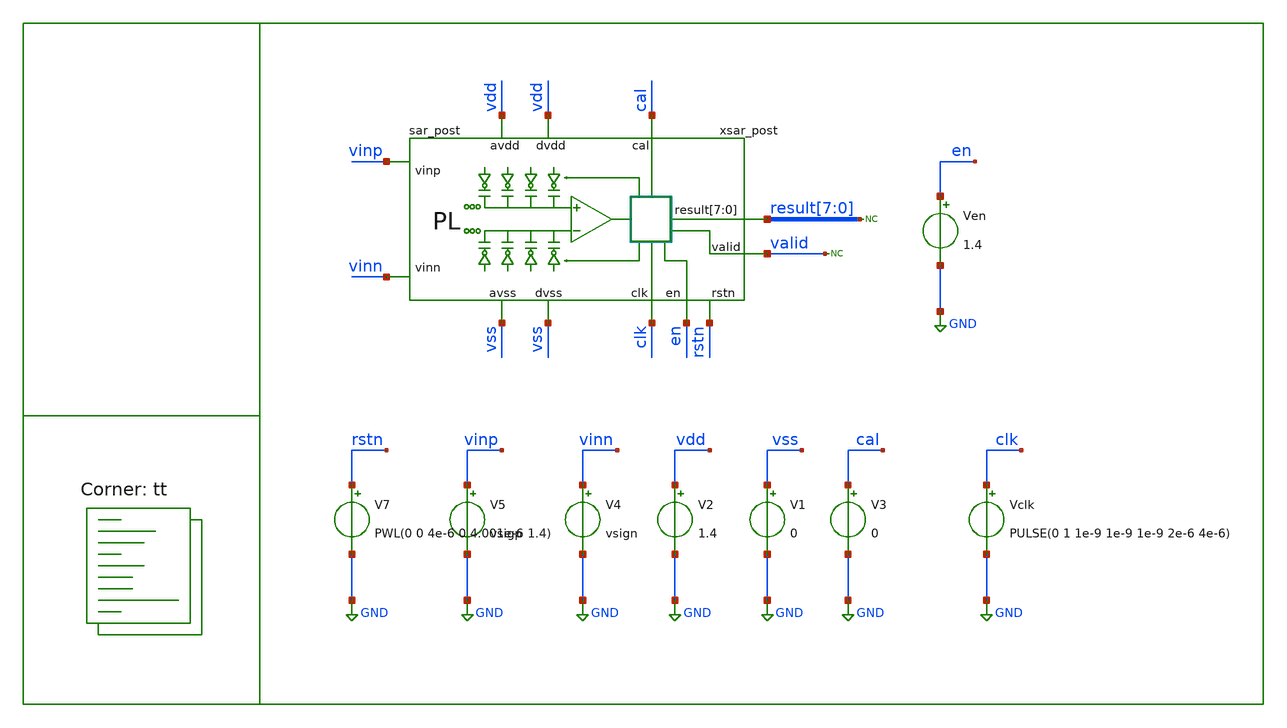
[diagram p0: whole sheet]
** sch_path: post_layout_separated/tr_sar_post.sch

.include /home/alex/Desktop/EDA/SAR_IPN/post_layout_separated/extracted.spice
.include /home/alex/Desktop/EDA/SAR_IPN/post_layout_separated/sar/control/cmos_cells_digital.sp
.include /home/alex/Desktop/EDA/SAR_IPN/post_layout_separated/sar/control/sar_logic.sp
.include $::SKYWATER_STDCELLS/sky130_fd_sc_hd.spice

.lib $::SKYWATER_MODELS/sky130.lib.spice tt
**.subckt tr_sar_post
V1 vss GND 0
V2 vdd GND 1.4
V4 vinn GND vsign
V5 vinp GND vsigp
Vclk clk GND PULSE(0 1 1e-9 1e-9 1e-9 2e-6 4e-6)
Ven en GND 1.4
* noconn valid
V3 cal GND 0
* noconn result[7:0]
xsar_post vdd vdd vss result[7] result[6] result[5] result[4] result[3] result[2] result[1]
+ result[0] vinn vss clk vinp en valid cal rstn sar_post
V7 rstn GND PWL(0 0 4e-6 0 4.001e-6 1.4)
**.ends
.GLOBAL GND
**** begin user architecture code

.options method trap
*.options method gear
.options gmin 1e-15
.options abstol 1e-15
.options reltol 0.0001
.options vntol 0.1e-6
.options warn 1

.param MC_SWITCH=0
.param vin=0.1
.param vcm=0.7
.param vsigp={vcm + vin/2}
.param vsign={vcm - vin/2}

.tran 100e-9 48e-6
.save all
.control

run
write tr_sar_post.raw
meas tran d0 find v(xsar_post.res0) at=47e-6
meas tran d1 find v(xsar_post.res1) at=47e-6
meas tran d2 find v(xsar_post.res2) at=47e-6
meas tran d3 find v(xsar_post.res3) at=47e-6
meas tran d4 find v(xsar_post.res4) at=47e-6
meas tran d5 find v(xsar_post.res5) at=47e-6
meas tran d6 find v(xsar_post.res6) at=47e-6
meas tran d7 find v(xsar_post.res7) at=47e-6

* meas tran d0 find v(xsar.result0) at=47e-6
* meas tran d1 find v(xsar.result1) at=47e-6
* meas tran d2 find v(xsar.result2) at=47e-6
* meas tran d3 find v(xsar.result3) at=47e-6
* meas tran d4 find v(xsar.result4) at=47e-6
* meas tran d5 find v(xsar.result5) at=47e-6
* meas tran d6 find v(xsar.result6) at=47e-6
* meas tran d7 find v(xsar.result7) at=47e-6

meas tran vpmax max xsar_post.vp
meas tran vpmin min xsar_post.vp
meas tran vpend find v(xsar_post.vp) at=39e-6

meas tran vnmax max xsar_post.vn
meas tran vnmin min xsar_post.vn
meas tran vnend find v(xsar_post.vn) at=39e-6

print d0
print d1
print d2
print d3
print d4
print d5
print d6
print d7

print vpmax
print vpmin

print vnmax
print vnmin

print vpend
print vnend

.endc


**** end user architecture code
.end
